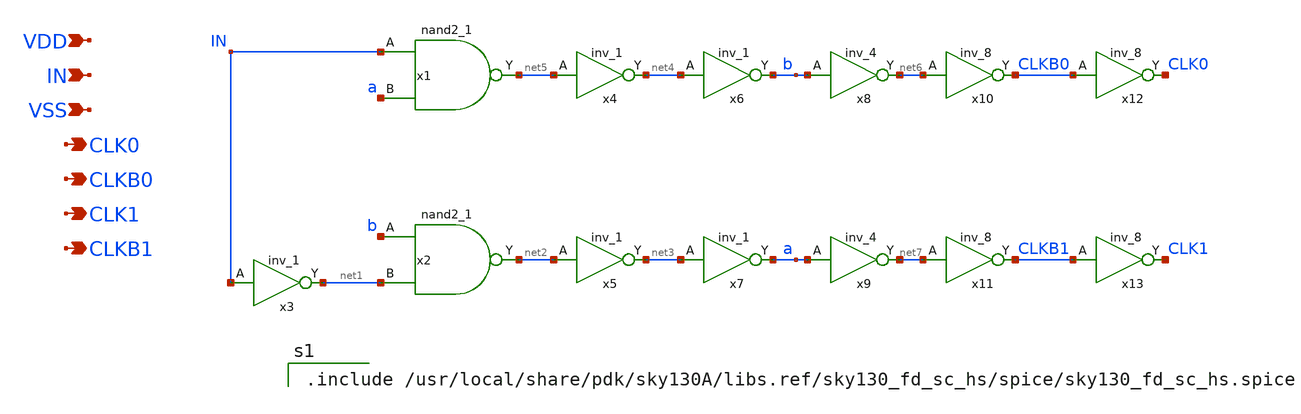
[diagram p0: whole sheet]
** sch_path: xschem/nooverlap_clk.sch
**.subckt nooverlap_clk VDD IN VSS CLK0 CLKB0 CLK1 CLKB1
*.ipin VDD
*.ipin IN
*.ipin VSS
*.opin CLK0
*.opin CLKB0
*.opin CLK1
*.opin CLKB1
x1 IN a vss vss vdd vdd net5 sky130_fd_sc_hs__nand2_1
x2 b net1 vss vss vdd vdd net2 sky130_fd_sc_hs__nand2_1
x3 IN vss vss vdd vdd net1 sky130_fd_sc_hs__inv_1
x4 net5 vss vss vdd vdd net4 sky130_fd_sc_hs__inv_1
x5 net2 vss vss vdd vdd net3 sky130_fd_sc_hs__inv_1
x6 net4 vss vss vdd vdd b sky130_fd_sc_hs__inv_1
x7 net3 vss vss vdd vdd a sky130_fd_sc_hs__inv_1
x8 b vss vss vdd vdd net6 sky130_fd_sc_hs__inv_4
x9 a vss vss vdd vdd net7 sky130_fd_sc_hs__inv_4
x10 net6 vss vss vdd vdd CLKB0 sky130_fd_sc_hs__inv_8
x11 net7 vss vss vdd vdd CLKB1 sky130_fd_sc_hs__inv_8
x12 CLKB0 vss vss vdd vdd CLK0 sky130_fd_sc_hs__inv_8
x13 CLKB1 vss vss vdd vdd CLK1 sky130_fd_sc_hs__inv_8
**** begin user architecture code

.include /usr/local/share/pdk/sky130A/libs.ref/sky130_fd_sc_hs/spice/sky130_fd_sc_hs.spice

**** end user architecture code
**.ends
.end
